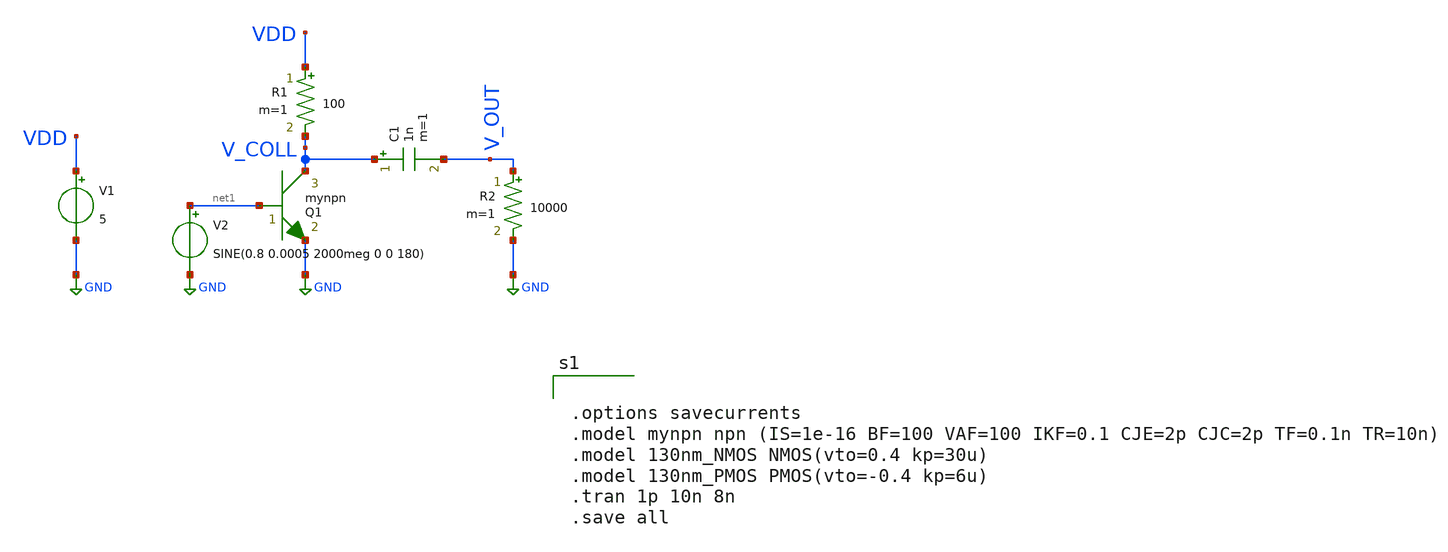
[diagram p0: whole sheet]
** sch_path: latchup/common_emitter.sch
**.subckt common_emitter
Q1 V_COLL net1 GND mynpn area=1 m=1
V1 VDD GND 5
R1 VDD V_COLL 100 m=1
V2 net1 GND SINE(0.8 0.0005 2000meg 0 0 180)
R2 V_OUT GND 10000 m=1
C1 V_COLL V_OUT 1n m=1
**** begin user architecture code


.options savecurrents
.model mynpn npn (IS=1e-16 BF=100 VAF=100 IKF=0.1 CJE=2p CJC=2p TF=0.1n TR=10n)
.model 130nm_NMOS NMOS(vto=0.4 kp=30u)
.model 130nm_PMOS PMOS(vto=-0.4 kp=6u)
.tran 1p 10n 8n
.save all




.include /usr/local/share/rad_modeling_blocks/rad_modeling_blocks.spice


**** end user architecture code
**.ends
.GLOBAL GND
.end
